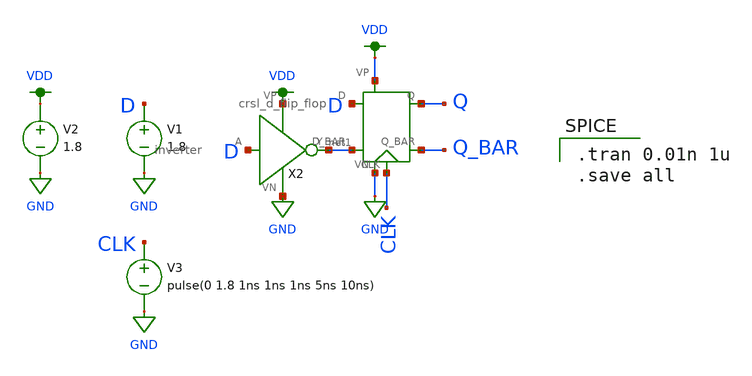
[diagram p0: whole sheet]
** sch_path: mp2/schematics/crsl_d_flip_flop_tran.sch
**.subckt crsl_d_flip_flop_tran
V1 D GND 1.8
X1 D net1 Q_BAR VDD Q CLK GND crsl_d_flip_flop
X2 D VDD GND net1 inverter
V2 VDD GND 1.8
V3 CLK GND pulse(0 1.8 1ns 1ns 1ns 5ns 10ns)
**** begin user architecture code

.option wnflag=1
.lib ~/skywater/skywater-pdk/libraries/sky130_fd_pr_ngspice/latest/models/sky130.lib.spice tt


.tran 0.01n 1u
.save all

**** end user architecture code
**.ends
.GLOBAL GND
.GLOBAL VDD
.end
